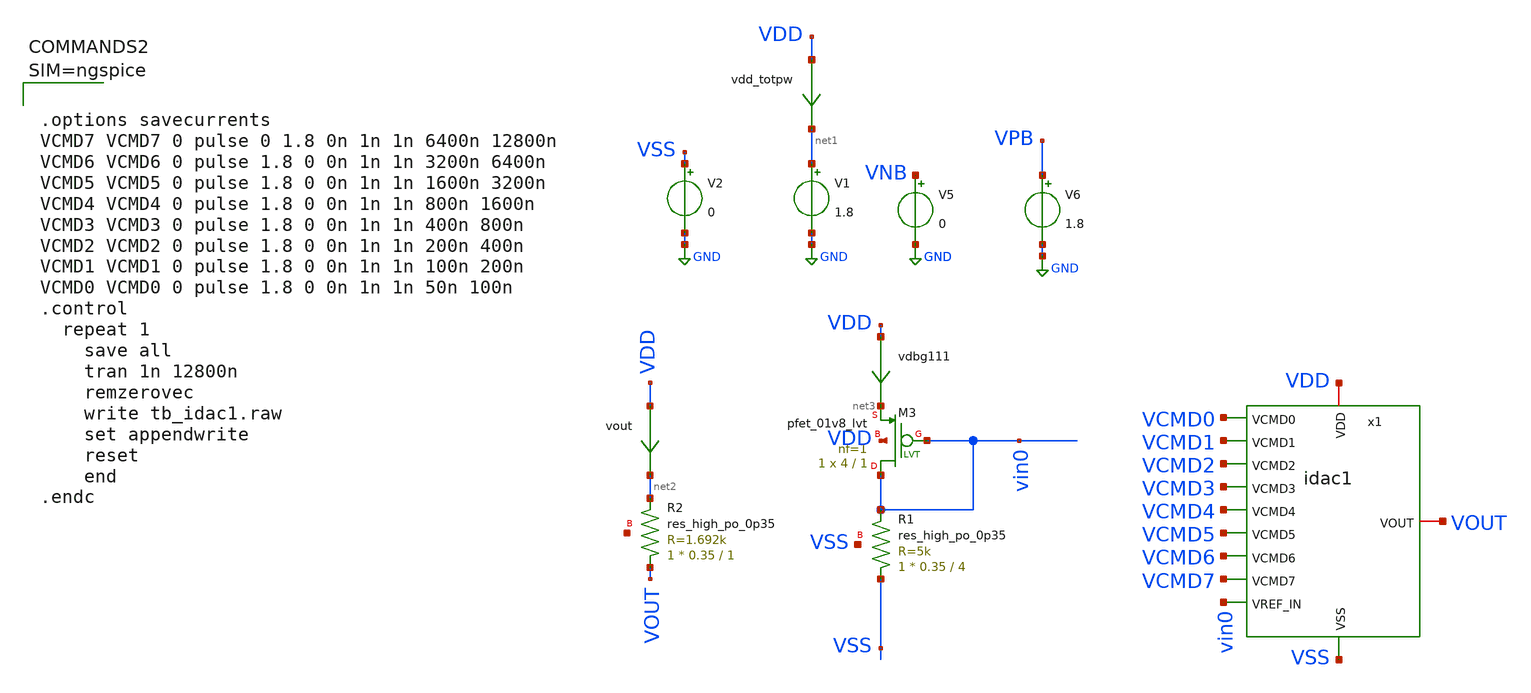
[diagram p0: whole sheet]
** sch_path: xschem/tb_idac1.sch
**.subckt tb_idac1
V5 VNB GND 0
V6 VPB GND 1.8
V1 net1 GND 1.8
V2 VSS GND 0
XM3 vin0 vin0 net3 VDD sky130_fd_pr__pfet_01v8_lvt L=1 W=4 nf=1 ad='int((nf+1)/2) * W/nf * 0.29' as='int((nf+2)/2) * W/nf * 0.29'
+ pd='2*int((nf+1)/2) * (W/nf + 0.29)' ps='2*int((nf+2)/2) * (W/nf + 0.29)' nrd='0.29 / W' nrs='0.29 / W'
+ sa=0 sb=0 sd=0 mult=1 m=1
vout VDD net2 0
.save i(vout)
XR1 VSS vin0 VSS sky130_fd_pr__res_high_po_0p35 L=4 mult=1 m=1
vdbg111 VDD net3 0
.save i(vdbg111)
XR2 VOUT net2 net4 sky130_fd_pr__res_high_po_0p35 L=1 mult=1 m=1
vdd_totpw VDD net1 0
.save i(vdd_totpw)
x1 VCMD0 VCMD1 VCMD2 VCMD3 VCMD4 VCMD5 VCMD6 VCMD7 VDD VOUT vin0 VSS idac1
**** begin user architecture code

** opencircuitdesign pdks install
.lib $::SKYWATER_MODELS/sky130.lib.spice tt_mm
*.lib $::SKYWATER_STDCELLS/sky130_fd_sc_hd_blablabla.spice

.subckt sky130_fd_sc_hd__inv_1 A VGND VNB VPB VPWR Y
X0 VGND A Y VNB sky130_fd_pr__nfet_01v8 w=650000u l=150000u
X1 VPWR A Y VPB sky130_fd_pr__pfet_01v8_hvt w=1e+06u l=150000u
.ends





.options savecurrents
VCMD7 VCMD7 0 pulse 0 1.8 0n 1n 1n 6400n 12800n
VCMD6 VCMD6 0 pulse 1.8 0 0n 1n 1n 3200n 6400n
VCMD5 VCMD5 0 pulse 1.8 0 0n 1n 1n 1600n 3200n
VCMD4 VCMD4 0 pulse 1.8 0 0n 1n 1n 800n 1600n
VCMD3 VCMD3 0 pulse 1.8 0 0n 1n 1n 400n 800n
VCMD2 VCMD2 0 pulse 1.8 0 0n 1n 1n 200n 400n
VCMD1 VCMD1 0 pulse 1.8 0 0n 1n 1n 100n 200n
VCMD0 VCMD0 0 pulse 1.8 0 0n 1n 1n 50n 100n
.control
  repeat 1
    save all
    tran 1n 12800n
    remzerovec
    write tb_idac1.raw
    set appendwrite
    reset
    end
.endc



**** end user architecture code
**.ends

* expanding   symbol:  idac1.sym # of pins=12
** sym_path: xschem/idac1.sym
** sch_path: xschem/idac1.sch
.subckt idac1 VCMD0 VCMD1 VCMD2 VCMD3 VCMD4 VCMD5 VCMD6 VCMD7 VDD VOUT VREF_IN VSS
*.ipin VSS
*.ipin VREF_IN
*.iopin VOUT
*.iopin VDD
*.ipin VCMD7
*.ipin VCMD6
*.ipin VCMD5
*.ipin VCMD4
*.ipin VCMD3
*.ipin VCMD2
*.ipin VCMD1
*.ipin VCMD0
xcell7 vin6 vin7 VOUT VDD VSS VCMD0 idac1cell
xcell6 vin5 vin6 VOUT VDD VSS VCMD1 idac1cell
xcell5 vin4 vin5 VOUT VDD VSS VCMD2 idac1cell
xcell4 vin3 vin4 VOUT VDD VSS VCMD3 idac1cell
xcell3 vin2 vin3 VOUT VDD VSS VCMD4 idac1cell
xcell2 vin1 vin2 VOUT VDD VSS VCMD5 idac1cell
xcell1 vin0 vin1 VOUT VDD VSS VCMD6 idac1cell
xcell0 VREF_IN vin0 VOUT VDD VSS VCMD7 idac1cell
.ends


* expanding   symbol:  idac1cell.sym # of pins=6
** sym_path: idac1cell.sym
** sch_path: idac1cell.sch
.subckt idac1cell VREF_IN VREF_OUT IOUT VDD VSS OE
*.ipin VSS
*.iopin VREF_OUT
*.ipin VREF_IN
*.iopin VDD
*.iopin IOUT
*.ipin OE
XM25 net1 net1 net3 VSS sky130_fd_pr__nfet_01v8_lvt L=1 W=4 nf=1 ad='int((nf+1)/2) * W/nf * 0.29' as='int((nf+2)/2) * W/nf * 0.29'
+ pd='2*int((nf+1)/2) * (W/nf + 0.29)' ps='2*int((nf+2)/2) * (W/nf + 0.29)' nrd='0.29 / W' nrs='0.29 / W'
+ sa=0 sb=0 sd=0 mult=1 m=1
XM26 net1 net1 VSS VSS sky130_fd_pr__nfet_01v8_lvt L=1 W=4 nf=1 ad='int((nf+1)/2) * W/nf * 0.29' as='int((nf+2)/2) * W/nf * 0.29'
+ pd='2*int((nf+1)/2) * (W/nf + 0.29)' ps='2*int((nf+2)/2) * (W/nf + 0.29)' nrd='0.29 / W' nrs='0.29 / W'
+ sa=0 sb=0 sd=0 mult=1 m=1
XM27 net1 VREF_IN VDD VDD sky130_fd_pr__pfet_01v8_lvt L=1 W=8 nf=1 ad='int((nf+1)/2) * W/nf * 0.29' as='int((nf+2)/2) * W/nf * 0.29'
+ pd='2*int((nf+1)/2) * (W/nf + 0.29)' ps='2*int((nf+2)/2) * (W/nf + 0.29)' nrd='0.29 / W' nrs='0.29 / W'
+ sa=0 sb=0 sd=0 mult=1 m=1
XM28 net4 net1 VSS VSS sky130_fd_pr__nfet_01v8_lvt L=1 W=4 nf=1 ad='int((nf+1)/2) * W/nf * 0.29' as='int((nf+2)/2) * W/nf * 0.29'
+ pd='2*int((nf+1)/2) * (W/nf + 0.29)' ps='2*int((nf+2)/2) * (W/nf + 0.29)' nrd='0.29 / W' nrs='0.29 / W'
+ sa=0 sb=0 sd=0 mult=1 m=1
XM29 VREF_OUT VREF_OUT VDD VDD sky130_fd_pr__pfet_01v8_lvt L=1 W=8 nf=1 ad='int((nf+1)/2) * W/nf * 0.29'
+ as='int((nf+2)/2) * W/nf * 0.29' pd='2*int((nf+1)/2) * (W/nf + 0.29)' ps='2*int((nf+2)/2) * (W/nf + 0.29)'
+ nrd='0.29 / W' nrs='0.29 / W' sa=0 sb=0 sd=0 mult=1 m=1
XM30 vdrain2 net1 VSS VSS sky130_fd_pr__nfet_01v8_lvt L=1 W=4 nf=1 ad='int((nf+1)/2) * W/nf * 0.29' as='int((nf+2)/2) * W/nf * 0.29'
+ pd='2*int((nf+1)/2) * (W/nf + 0.29)' ps='2*int((nf+2)/2) * (W/nf + 0.29)' nrd='0.29 / W' nrs='0.29 / W'
+ sa=0 sb=0 sd=0 mult=1 m=1
XM31 net2 OE vdrain2 VSS sky130_fd_pr__nfet_01v8_lvt L=1 W=4 nf=1 ad='int((nf+1)/2) * W/nf * 0.29' as='int((nf+2)/2) * W/nf * 0.29'
+ pd='2*int((nf+1)/2) * (W/nf + 0.29)' ps='2*int((nf+2)/2) * (W/nf + 0.29)' nrd='0.29 / W' nrs='0.29 / W'
+ sa=0 sb=0 sd=0 mult=1 m=1
vref net3 VSS 0
.save i(vref)
viout IOUT net2 0
.save i(viout)
vmeas VREF_OUT net4 0
.save i(vmeas)
.ends

.GLOBAL GND
.end
